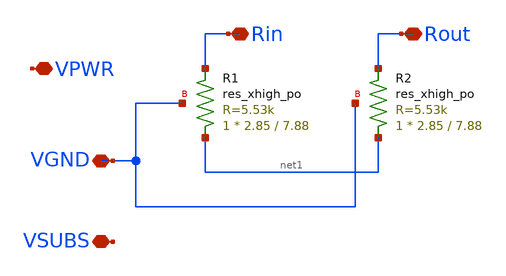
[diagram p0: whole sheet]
** sch_path: xschem/xschem/analog_stdcells/skywater_asc_res_xhigh_po_2p85_1.sch
**.subckt skywater_asc_res_xhigh_po_2p85_1 Rin Rout VPWR VGND VSUBS
*.iopin Rin
*.iopin Rout
*.iopin VPWR
*.iopin VGND
*.iopin VSUBS
XR1 net1 Rin VGND sky130_fd_pr__res_xhigh_po W=2.85 L=7.88 mult=1 m=1
XR2 net1 Rout VGND sky130_fd_pr__res_xhigh_po W=2.85 L=7.88 mult=1 m=1
**.ends
.end
